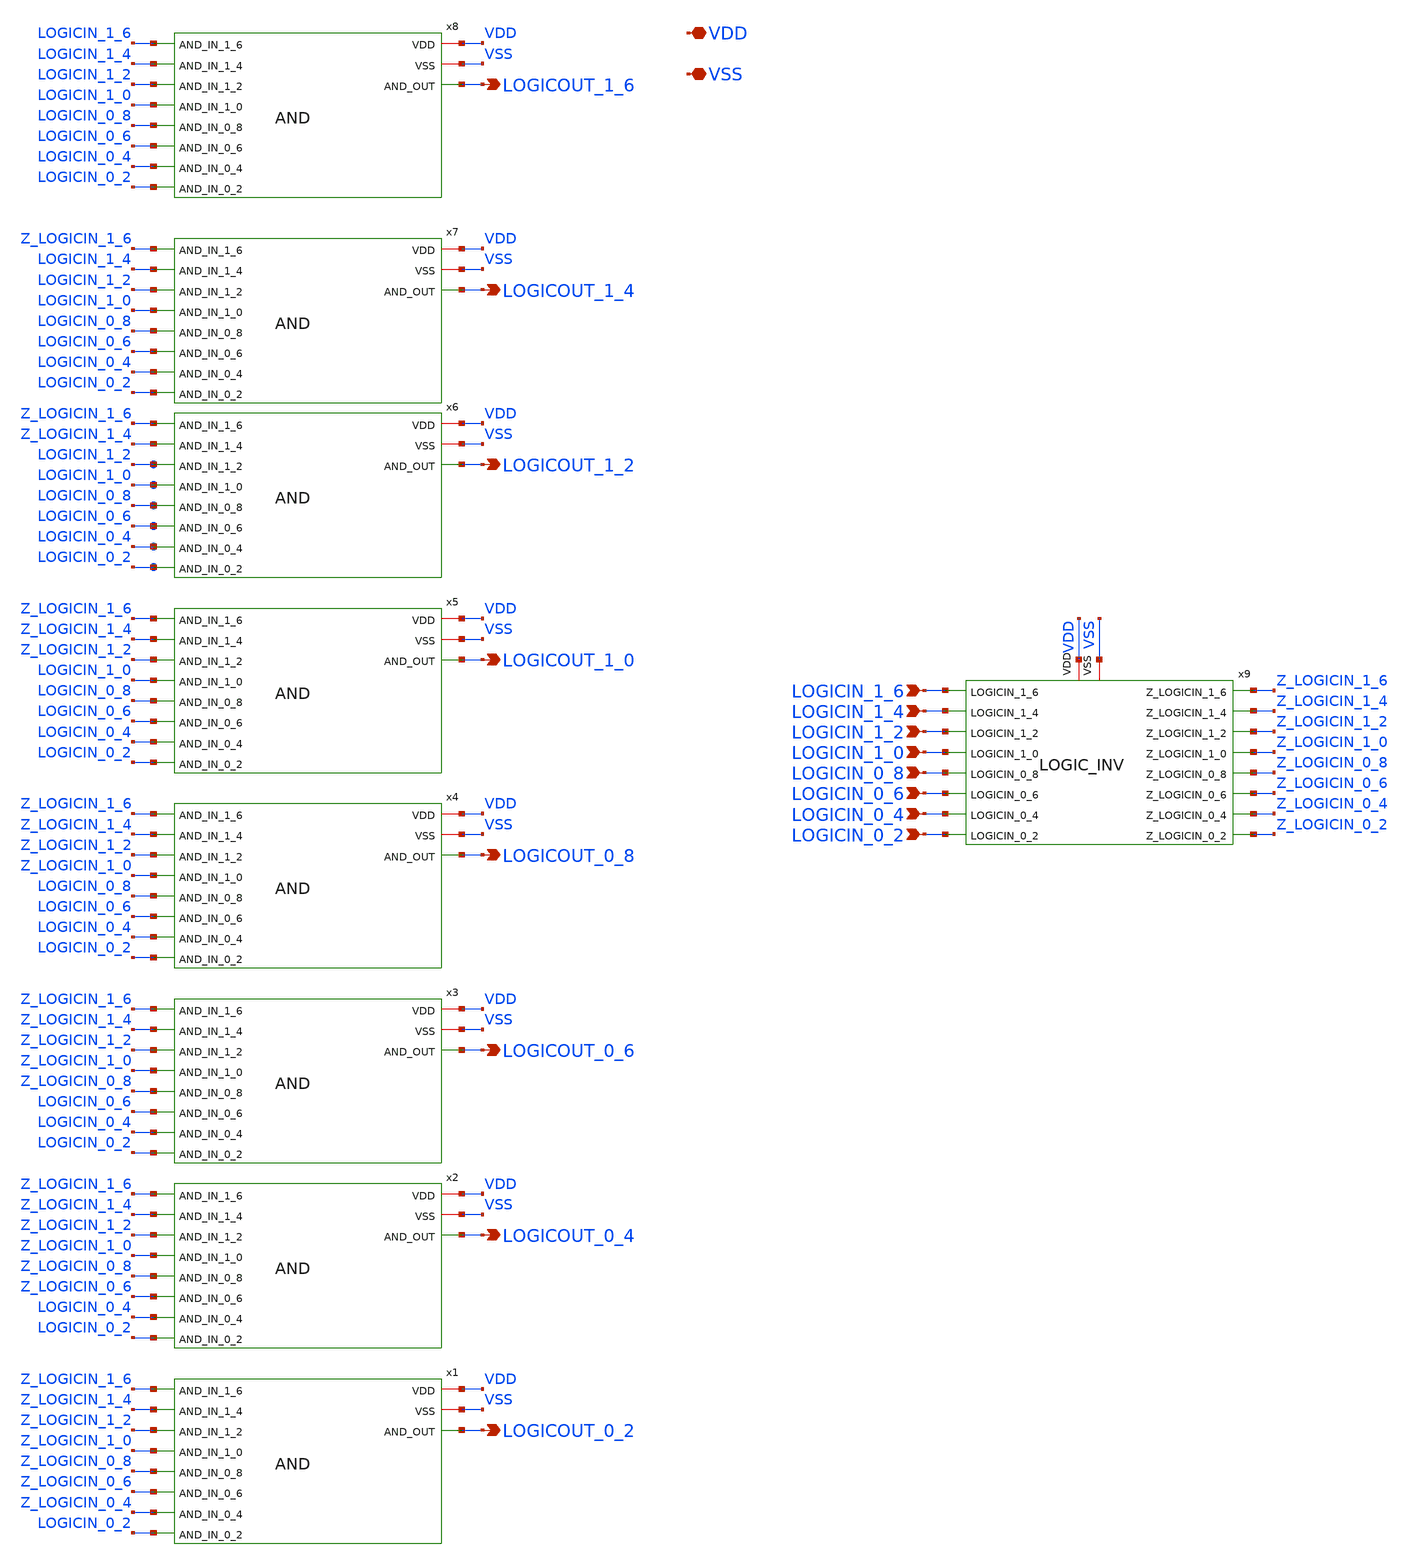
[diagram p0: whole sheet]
** sch_path: xschem/LOGIC.sch
**.subckt LOGIC LOGICOUT_0_2 LOGICOUT_0_4 LOGICOUT_0_6 LOGICOUT_0_8 LOGICOUT_1_0 LOGICOUT_1_2
*+ LOGICOUT_1_4 LOGICOUT_1_6 LOGICIN_1_0 LOGICIN_1_2 LOGICIN_1_4 LOGICIN_1_6 LOGICIN_0_2 LOGICIN_0_4 LOGICIN_0_6
*+ LOGICIN_0_8 VDD VSS
*.opin LOGICOUT_0_2
*.opin LOGICOUT_0_4
*.opin LOGICOUT_0_6
*.opin LOGICOUT_0_8
*.opin LOGICOUT_1_0
*.opin LOGICOUT_1_2
*.opin LOGICOUT_1_4
*.opin LOGICOUT_1_6
*.ipin LOGICIN_1_0
*.ipin LOGICIN_1_2
*.ipin LOGICIN_1_4
*.ipin LOGICIN_1_6
*.ipin LOGICIN_0_2
*.ipin LOGICIN_0_4
*.ipin LOGICIN_0_6
*.ipin LOGICIN_0_8
*.iopin VDD
*.iopin VSS
x1 VDD VSS Z_LOGICIN_1_6 Z_LOGICIN_1_4 Z_LOGICIN_1_2 Z_LOGICIN_1_0 LOGICOUT_0_2 Z_LOGICIN_0_8
+ Z_LOGICIN_0_6 Z_LOGICIN_0_4 LOGICIN_0_2 AND
x2 VDD VSS Z_LOGICIN_1_6 Z_LOGICIN_1_4 Z_LOGICIN_1_2 Z_LOGICIN_1_0 LOGICOUT_0_4 Z_LOGICIN_0_8
+ Z_LOGICIN_0_6 LOGICIN_0_4 LOGICIN_0_2 AND
x3 VDD VSS Z_LOGICIN_1_6 Z_LOGICIN_1_4 Z_LOGICIN_1_2 Z_LOGICIN_1_0 LOGICOUT_0_6 Z_LOGICIN_0_8
+ LOGICIN_0_6 LOGICIN_0_4 LOGICIN_0_2 AND
x4 VDD VSS Z_LOGICIN_1_6 Z_LOGICIN_1_4 Z_LOGICIN_1_2 Z_LOGICIN_1_0 LOGICOUT_0_8 LOGICIN_0_8
+ LOGICIN_0_6 LOGICIN_0_4 LOGICIN_0_2 AND
x5 VDD VSS Z_LOGICIN_1_6 Z_LOGICIN_1_4 Z_LOGICIN_1_2 LOGICIN_1_0 LOGICOUT_1_0 LOGICIN_0_8
+ LOGICIN_0_6 LOGICIN_0_4 LOGICIN_0_2 AND
x6 VDD VSS Z_LOGICIN_1_6 Z_LOGICIN_1_4 LOGICIN_1_2 LOGICIN_1_0 LOGICOUT_1_2 LOGICIN_0_8 LOGICIN_0_6
+ LOGICIN_0_4 LOGICIN_0_2 AND
x7 VDD VSS Z_LOGICIN_1_6 LOGICIN_1_4 LOGICIN_1_2 LOGICIN_1_0 LOGICOUT_1_4 LOGICIN_0_8 LOGICIN_0_6
+ LOGICIN_0_4 LOGICIN_0_2 AND
x8 VDD VSS LOGICIN_1_6 LOGICIN_1_4 LOGICIN_1_2 LOGICIN_1_0 LOGICOUT_1_6 LOGICIN_0_8 LOGICIN_0_6
+ LOGICIN_0_4 LOGICIN_0_2 AND
x9 LOGICIN_1_6 Z_LOGICIN_1_6 Z_LOGICIN_1_4 LOGICIN_1_4 LOGICIN_1_2 Z_LOGICIN_1_2 LOGICIN_1_0
+ Z_LOGICIN_1_0 Z_LOGICIN_0_8 LOGICIN_0_8 Z_LOGICIN_0_6 LOGICIN_0_6 LOGICIN_0_4 Z_LOGICIN_0_4 LOGICIN_0_2
+ Z_LOGICIN_0_2 VDD VSS LOGIC_INV
**.ends
.end
